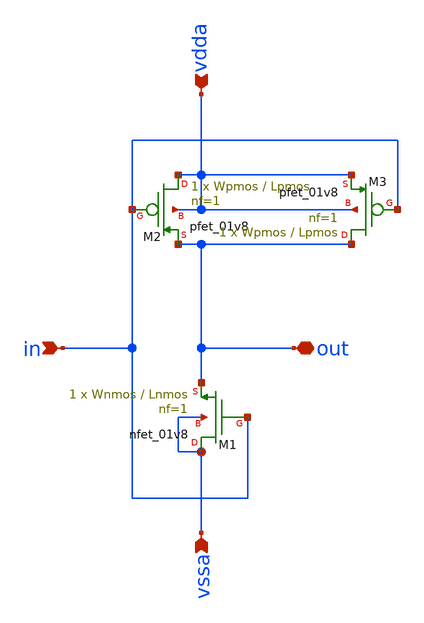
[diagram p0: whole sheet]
** sch_path: xschem/inv/inv.sch
**.subckt inv in out vdda vssa
*.ipin in
*.iopin out
*.ipin vdda
*.ipin vssa
XM1 vssa in out vssa sky130_fd_pr__nfet_01v8 L=Lnmos W=Wnmos nf=1 ad='int((nf+1)/2) * W/nf * 0.29' as='int((nf+2)/2) * W/nf * 0.29'
+ pd='2*int((nf+1)/2) * (W/nf + 0.29)' ps='2*int((nf+2)/2) * (W/nf + 0.29)' nrd='0.29 / W' nrs='0.29 / W'
+ sa=0 sb=0 sd=0 mult=1 m=1
XM2 vdda in out vdda sky130_fd_pr__pfet_01v8 L=Lpmos W=Wpmos nf=1 ad='int((nf+1)/2) * W/nf * 0.29' as='int((nf+2)/2) * W/nf * 0.29'
+ pd='2*int((nf+1)/2) * (W/nf + 0.29)' ps='2*int((nf+2)/2) * (W/nf + 0.29)' nrd='0.29 / W' nrs='0.29 / W'
+ sa=0 sb=0 sd=0 mult=1 m=1
XM3 out in vdda vdda sky130_fd_pr__pfet_01v8 L=Lpmos W=Wpmos nf=1 ad='int((nf+1)/2) * W/nf * 0.29' as='int((nf+2)/2) * W/nf * 0.29'
+ pd='2*int((nf+1)/2) * (W/nf + 0.29)' ps='2*int((nf+2)/2) * (W/nf + 0.29)' nrd='0.29 / W' nrs='0.29 / W'
+ sa=0 sb=0 sd=0 mult=1 m=1
**.ends
.end
